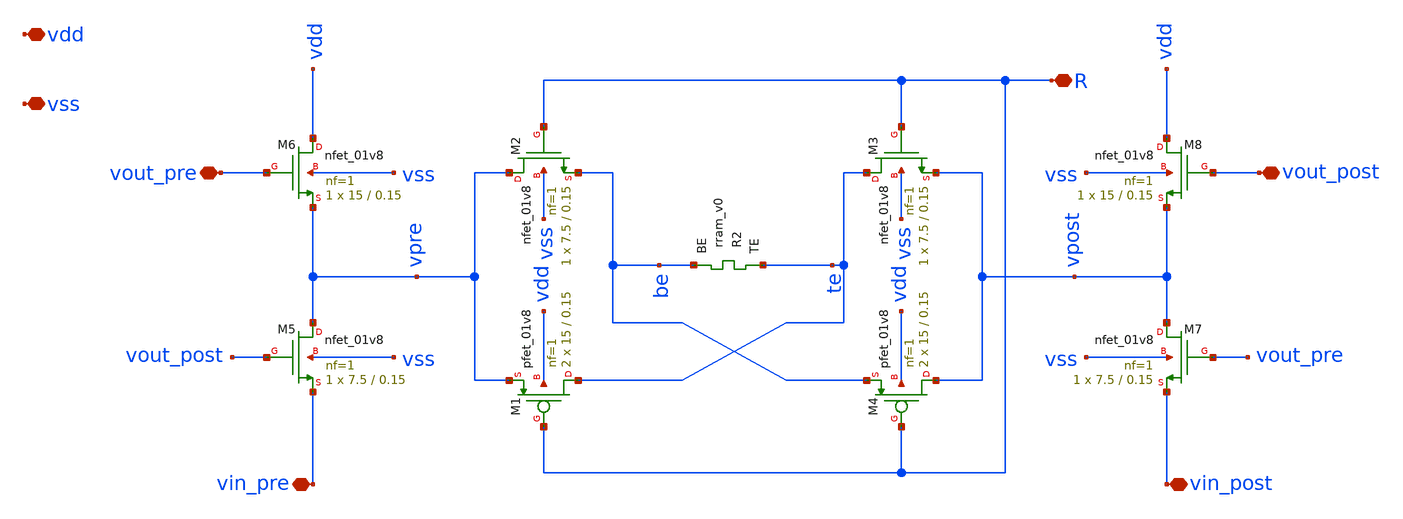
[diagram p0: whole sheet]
** sch_path: Synapse/rstdp_switched.sch
**.subckt rstdp_switched vdd vss R vout_post vout_pre vin_post vin_pre
*.iopin vdd
*.iopin vss
*.iopin R
*.iopin vout_post
*.iopin vout_pre
*.iopin vin_post
*.iopin vin_pre
XR2 te be rram_v0
XM2 vpre R be vss sky130_fd_pr__nfet_01v8 L=0.15 W=7.5 nf=1 ad='int((nf+1)/2) * W/nf * 0.29' as='int((nf+2)/2) * W/nf * 0.29'
+ pd='2*int((nf+1)/2) * (W/nf + 0.29)' ps='2*int((nf+2)/2) * (W/nf + 0.29)' nrd='0.29 / W' nrs='0.29 / W'
+ sa=0 sb=0 sd=0 mult=1 m=1
XM3 te R vpost vss sky130_fd_pr__nfet_01v8 L=0.15 W=7.5 nf=1 ad='int((nf+1)/2) * W/nf * 0.29' as='int((nf+2)/2) * W/nf * 0.29'
+ pd='2*int((nf+1)/2) * (W/nf + 0.29)' ps='2*int((nf+2)/2) * (W/nf + 0.29)' nrd='0.29 / W' nrs='0.29 / W'
+ sa=0 sb=0 sd=0 mult=1 m=1
XM1 te R vpre vdd sky130_fd_pr__pfet_01v8 L=0.15 W=15 nf=1 ad='int((nf+1)/2) * W/nf * 0.29' as='int((nf+2)/2) * W/nf * 0.29'
+ pd='2*int((nf+1)/2) * (W/nf + 0.29)' ps='2*int((nf+2)/2) * (W/nf + 0.29)' nrd='0.29 / W' nrs='0.29 / W'
+ sa=0 sb=0 sd=0 mult=2 m=2
XM4 vpost R be vdd sky130_fd_pr__pfet_01v8 L=0.15 W=15 nf=1 ad='int((nf+1)/2) * W/nf * 0.29' as='int((nf+2)/2) * W/nf * 0.29'
+ pd='2*int((nf+1)/2) * (W/nf + 0.29)' ps='2*int((nf+2)/2) * (W/nf + 0.29)' nrd='0.29 / W' nrs='0.29 / W'
+ sa=0 sb=0 sd=0 mult=2 m=2
XM7 vpost vout_pre vin_post vss sky130_fd_pr__nfet_01v8 L=0.15 W=7.5 nf=1 ad='int((nf+1)/2) * W/nf * 0.29'
+ as='int((nf+2)/2) * W/nf * 0.29' pd='2*int((nf+1)/2) * (W/nf + 0.29)' ps='2*int((nf+2)/2) * (W/nf + 0.29)'
+ nrd='0.29 / W' nrs='0.29 / W' sa=0 sb=0 sd=0 mult=1 m=1
XM8 vdd vout_post vpost vss sky130_fd_pr__nfet_01v8 L=0.15 W=15 nf=1 ad='int((nf+1)/2) * W/nf * 0.29'
+ as='int((nf+2)/2) * W/nf * 0.29' pd='2*int((nf+1)/2) * (W/nf + 0.29)' ps='2*int((nf+2)/2) * (W/nf + 0.29)'
+ nrd='0.29 / W' nrs='0.29 / W' sa=0 sb=0 sd=0 mult=1 m=1
XM5 vpre vout_post vin_pre vss sky130_fd_pr__nfet_01v8 L=0.15 W=7.5 nf=1 ad='int((nf+1)/2) * W/nf * 0.29'
+ as='int((nf+2)/2) * W/nf * 0.29' pd='2*int((nf+1)/2) * (W/nf + 0.29)' ps='2*int((nf+2)/2) * (W/nf + 0.29)'
+ nrd='0.29 / W' nrs='0.29 / W' sa=0 sb=0 sd=0 mult=1 m=1
XM6 vdd vout_pre vpre vss sky130_fd_pr__nfet_01v8 L=0.15 W=15 nf=1 ad='int((nf+1)/2) * W/nf * 0.29' as='int((nf+2)/2) * W/nf * 0.29'
+ pd='2*int((nf+1)/2) * (W/nf + 0.29)' ps='2*int((nf+2)/2) * (W/nf + 0.29)' nrd='0.29 / W' nrs='0.29 / W'
+ sa=0 sb=0 sd=0 mult=1 m=1
**.ends
.end
